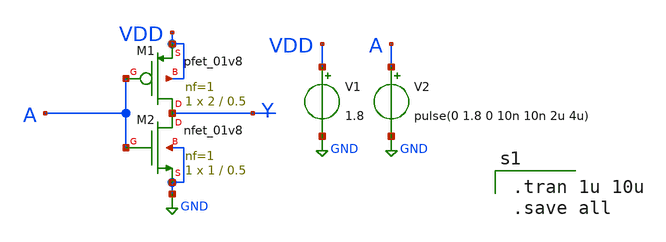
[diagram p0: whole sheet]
** sch_path: xschem_sky130/test_inverter.sch
**.subckt test_inverter
XM1 Y A VDD VDD sky130_fd_pr__pfet_01v8 L=0.5 W=2 nf=1 ad='int((nf+1)/2) * W/nf * 0.29' as='int((nf+2)/2) * W/nf * 0.29'
+ pd='2*int((nf+1)/2) * (W/nf + 0.29)' ps='2*int((nf+2)/2) * (W/nf + 0.29)' nrd='0.29 / W' nrs='0.29 / W'
+ sa=0 sb=0 sd=0 mult=1 m=1
XM2 Y A GND GND sky130_fd_pr__nfet_01v8 L=0.5 W=1 nf=1 ad='int((nf+1)/2) * W/nf * 0.29' as='int((nf+2)/2) * W/nf * 0.29'
+ pd='2*int((nf+1)/2) * (W/nf + 0.29)' ps='2*int((nf+2)/2) * (W/nf + 0.29)' nrd='0.29 / W' nrs='0.29 / W'
+ sa=0 sb=0 sd=0 mult=1 m=1
V1 VDD GND 1.8
V2 A GND pulse(0 1.8 0 10n 10n 2u 4u)
**** begin user architecture code

** opencircuitdesign pdks install
.lib $::SKYWATER_MODELS/sky130.lib.spice tt



.tran 1u 10u
.save all

**** end user architecture code
**.ends
.GLOBAL GND
.end
